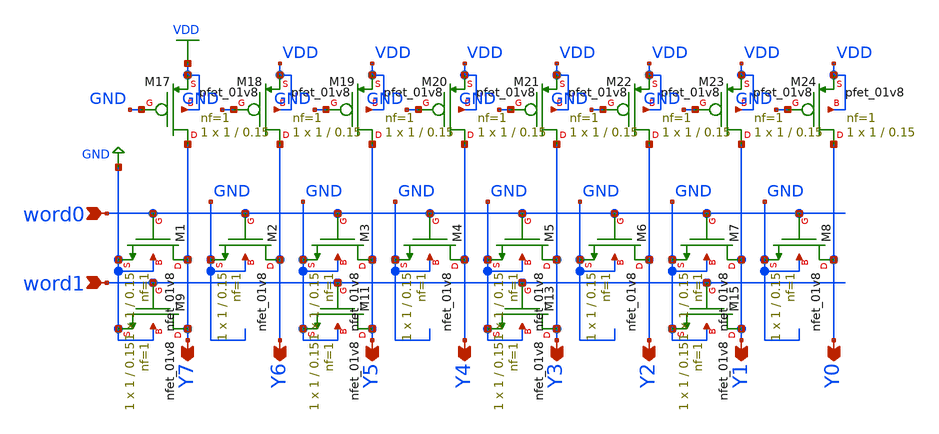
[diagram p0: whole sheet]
** sch_path: circuits/xschem/rom.sch
**.subckt rom word0 word1 Y7 Y6 Y5 Y4 Y3 Y2 Y1 Y0
*.ipin word0
*.ipin word1
*.opin Y7
*.opin Y6
*.opin Y5
*.opin Y4
*.opin Y3
*.opin Y2
*.opin Y1
*.opin Y0
XM9 Y7 word1 GND GND sky130_fd_pr__nfet_01v8 L=0.15 W=1 nf=1 ad='int((nf+1)/2) * W/nf * 0.29' as='int((nf+2)/2) * W/nf * 0.29'
+ pd='2*int((nf+1)/2) * (W/nf + 0.29)' ps='2*int((nf+2)/2) * (W/nf + 0.29)' nrd='0.29 / W' nrs='0.29 / W'
+ sa=0 sb=0 sd=0 mult=1 m=1
XM1 Y7 word0 GND GND sky130_fd_pr__nfet_01v8 L=0.15 W=1 nf=1 ad='int((nf+1)/2) * W/nf * 0.29' as='int((nf+2)/2) * W/nf * 0.29'
+ pd='2*int((nf+1)/2) * (W/nf + 0.29)' ps='2*int((nf+2)/2) * (W/nf + 0.29)' nrd='0.29 / W' nrs='0.29 / W'
+ sa=0 sb=0 sd=0 mult=1 m=1
XM2 Y6 word0 GND GND sky130_fd_pr__nfet_01v8 L=0.15 W=1 nf=1 ad='int((nf+1)/2) * W/nf * 0.29' as='int((nf+2)/2) * W/nf * 0.29'
+ pd='2*int((nf+1)/2) * (W/nf + 0.29)' ps='2*int((nf+2)/2) * (W/nf + 0.29)' nrd='0.29 / W' nrs='0.29 / W'
+ sa=0 sb=0 sd=0 mult=1 m=1
XM3 Y5 word0 GND GND sky130_fd_pr__nfet_01v8 L=0.15 W=1 nf=1 ad='int((nf+1)/2) * W/nf * 0.29' as='int((nf+2)/2) * W/nf * 0.29'
+ pd='2*int((nf+1)/2) * (W/nf + 0.29)' ps='2*int((nf+2)/2) * (W/nf + 0.29)' nrd='0.29 / W' nrs='0.29 / W'
+ sa=0 sb=0 sd=0 mult=1 m=1
XM4 Y4 word0 GND GND sky130_fd_pr__nfet_01v8 L=0.15 W=1 nf=1 ad='int((nf+1)/2) * W/nf * 0.29' as='int((nf+2)/2) * W/nf * 0.29'
+ pd='2*int((nf+1)/2) * (W/nf + 0.29)' ps='2*int((nf+2)/2) * (W/nf + 0.29)' nrd='0.29 / W' nrs='0.29 / W'
+ sa=0 sb=0 sd=0 mult=1 m=1
XM5 Y3 word0 GND GND sky130_fd_pr__nfet_01v8 L=0.15 W=1 nf=1 ad='int((nf+1)/2) * W/nf * 0.29' as='int((nf+2)/2) * W/nf * 0.29'
+ pd='2*int((nf+1)/2) * (W/nf + 0.29)' ps='2*int((nf+2)/2) * (W/nf + 0.29)' nrd='0.29 / W' nrs='0.29 / W'
+ sa=0 sb=0 sd=0 mult=1 m=1
XM6 Y2 word0 GND GND sky130_fd_pr__nfet_01v8 L=0.15 W=1 nf=1 ad='int((nf+1)/2) * W/nf * 0.29' as='int((nf+2)/2) * W/nf * 0.29'
+ pd='2*int((nf+1)/2) * (W/nf + 0.29)' ps='2*int((nf+2)/2) * (W/nf + 0.29)' nrd='0.29 / W' nrs='0.29 / W'
+ sa=0 sb=0 sd=0 mult=1 m=1
XM7 Y1 word0 GND GND sky130_fd_pr__nfet_01v8 L=0.15 W=1 nf=1 ad='int((nf+1)/2) * W/nf * 0.29' as='int((nf+2)/2) * W/nf * 0.29'
+ pd='2*int((nf+1)/2) * (W/nf + 0.29)' ps='2*int((nf+2)/2) * (W/nf + 0.29)' nrd='0.29 / W' nrs='0.29 / W'
+ sa=0 sb=0 sd=0 mult=1 m=1
XM8 Y0 word0 GND GND sky130_fd_pr__nfet_01v8 L=0.15 W=1 nf=1 ad='int((nf+1)/2) * W/nf * 0.29' as='int((nf+2)/2) * W/nf * 0.29'
+ pd='2*int((nf+1)/2) * (W/nf + 0.29)' ps='2*int((nf+2)/2) * (W/nf + 0.29)' nrd='0.29 / W' nrs='0.29 / W'
+ sa=0 sb=0 sd=0 mult=1 m=1
XM11 Y5 word1 GND GND sky130_fd_pr__nfet_01v8 L=0.15 W=1 nf=1 ad='int((nf+1)/2) * W/nf * 0.29' as='int((nf+2)/2) * W/nf * 0.29'
+ pd='2*int((nf+1)/2) * (W/nf + 0.29)' ps='2*int((nf+2)/2) * (W/nf + 0.29)' nrd='0.29 / W' nrs='0.29 / W'
+ sa=0 sb=0 sd=0 mult=1 m=1
XM13 Y3 word1 GND GND sky130_fd_pr__nfet_01v8 L=0.15 W=1 nf=1 ad='int((nf+1)/2) * W/nf * 0.29' as='int((nf+2)/2) * W/nf * 0.29'
+ pd='2*int((nf+1)/2) * (W/nf + 0.29)' ps='2*int((nf+2)/2) * (W/nf + 0.29)' nrd='0.29 / W' nrs='0.29 / W'
+ sa=0 sb=0 sd=0 mult=1 m=1
XM15 Y1 word1 GND GND sky130_fd_pr__nfet_01v8 L=0.15 W=1 nf=1 ad='int((nf+1)/2) * W/nf * 0.29' as='int((nf+2)/2) * W/nf * 0.29'
+ pd='2*int((nf+1)/2) * (W/nf + 0.29)' ps='2*int((nf+2)/2) * (W/nf + 0.29)' nrd='0.29 / W' nrs='0.29 / W'
+ sa=0 sb=0 sd=0 mult=1 m=1
XM17 Y7 GND VDD VDD sky130_fd_pr__pfet_01v8 L=0.15 W=1 nf=1 ad='int((nf+1)/2) * W/nf * 0.29' as='int((nf+2)/2) * W/nf * 0.29'
+ pd='2*int((nf+1)/2) * (W/nf + 0.29)' ps='2*int((nf+2)/2) * (W/nf + 0.29)' nrd='0.29 / W' nrs='0.29 / W'
+ sa=0 sb=0 sd=0 mult=1 m=1
XM18 Y6 GND VDD VDD sky130_fd_pr__pfet_01v8 L=0.15 W=1 nf=1 ad='int((nf+1)/2) * W/nf * 0.29' as='int((nf+2)/2) * W/nf * 0.29'
+ pd='2*int((nf+1)/2) * (W/nf + 0.29)' ps='2*int((nf+2)/2) * (W/nf + 0.29)' nrd='0.29 / W' nrs='0.29 / W'
+ sa=0 sb=0 sd=0 mult=1 m=1
XM19 Y5 GND VDD VDD sky130_fd_pr__pfet_01v8 L=0.15 W=1 nf=1 ad='int((nf+1)/2) * W/nf * 0.29' as='int((nf+2)/2) * W/nf * 0.29'
+ pd='2*int((nf+1)/2) * (W/nf + 0.29)' ps='2*int((nf+2)/2) * (W/nf + 0.29)' nrd='0.29 / W' nrs='0.29 / W'
+ sa=0 sb=0 sd=0 mult=1 m=1
XM20 Y4 GND VDD VDD sky130_fd_pr__pfet_01v8 L=0.15 W=1 nf=1 ad='int((nf+1)/2) * W/nf * 0.29' as='int((nf+2)/2) * W/nf * 0.29'
+ pd='2*int((nf+1)/2) * (W/nf + 0.29)' ps='2*int((nf+2)/2) * (W/nf + 0.29)' nrd='0.29 / W' nrs='0.29 / W'
+ sa=0 sb=0 sd=0 mult=1 m=1
XM21 Y3 GND VDD VDD sky130_fd_pr__pfet_01v8 L=0.15 W=1 nf=1 ad='int((nf+1)/2) * W/nf * 0.29' as='int((nf+2)/2) * W/nf * 0.29'
+ pd='2*int((nf+1)/2) * (W/nf + 0.29)' ps='2*int((nf+2)/2) * (W/nf + 0.29)' nrd='0.29 / W' nrs='0.29 / W'
+ sa=0 sb=0 sd=0 mult=1 m=1
XM22 Y2 GND VDD VDD sky130_fd_pr__pfet_01v8 L=0.15 W=1 nf=1 ad='int((nf+1)/2) * W/nf * 0.29' as='int((nf+2)/2) * W/nf * 0.29'
+ pd='2*int((nf+1)/2) * (W/nf + 0.29)' ps='2*int((nf+2)/2) * (W/nf + 0.29)' nrd='0.29 / W' nrs='0.29 / W'
+ sa=0 sb=0 sd=0 mult=1 m=1
XM23 Y1 GND VDD VDD sky130_fd_pr__pfet_01v8 L=0.15 W=1 nf=1 ad='int((nf+1)/2) * W/nf * 0.29' as='int((nf+2)/2) * W/nf * 0.29'
+ pd='2*int((nf+1)/2) * (W/nf + 0.29)' ps='2*int((nf+2)/2) * (W/nf + 0.29)' nrd='0.29 / W' nrs='0.29 / W'
+ sa=0 sb=0 sd=0 mult=1 m=1
XM24 Y0 GND VDD VDD sky130_fd_pr__pfet_01v8 L=0.15 W=1 nf=1 ad='int((nf+1)/2) * W/nf * 0.29' as='int((nf+2)/2) * W/nf * 0.29'
+ pd='2*int((nf+1)/2) * (W/nf + 0.29)' ps='2*int((nf+2)/2) * (W/nf + 0.29)' nrd='0.29 / W' nrs='0.29 / W'
+ sa=0 sb=0 sd=0 mult=1 m=1
**.ends
.GLOBAL GND
.GLOBAL VDD
.end
